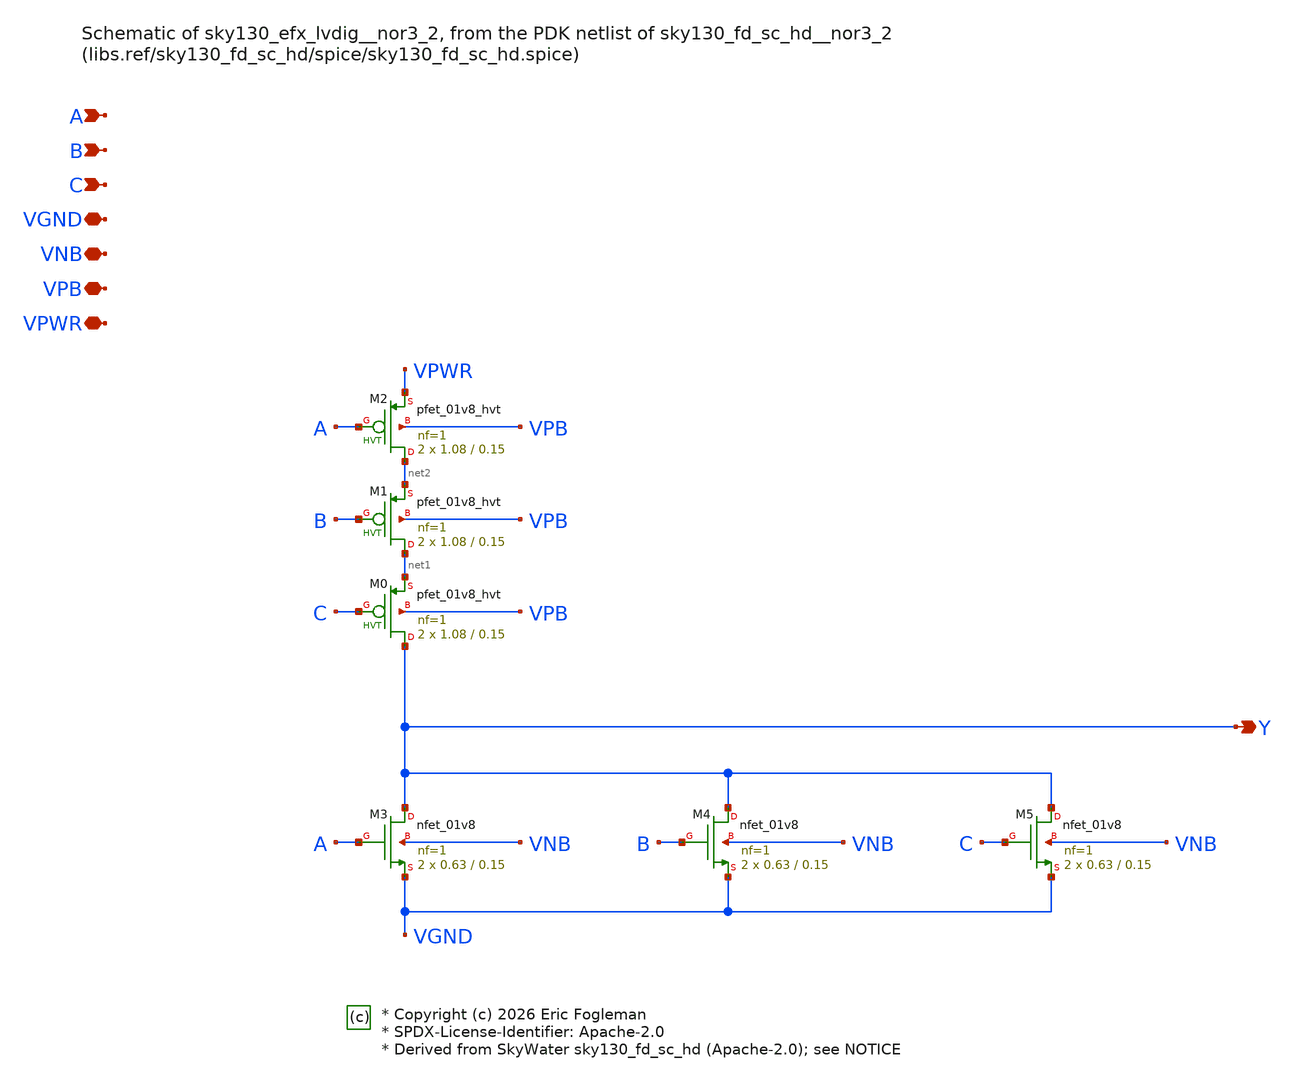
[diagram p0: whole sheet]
** sch_path: xschem/sky130_efx_lvdig__nor3_2.sch

* Copyright (c) 2026 Eric Fogleman
* SPDX-License-Identifier: Apache-2.0
* Derived from SkyWater sky130_fd_sc_hd (Apache-2.0); see NOTICE

**.subckt sky130_efx_lvdig__nor3_2 Y A B C VGND VNB VPB VPWR
*.opin Y
*.ipin A
*.ipin B
*.ipin C
*.iopin VGND
*.iopin VNB
*.iopin VPB
*.iopin VPWR
XM0 Y C net1 VPB sky130_fd_pr__pfet_01v8_hvt L=0.15 W=1.08 nf=1 ad='int((1 + 1)/2) * 1.08 / 1 * 0.29'
+ as='int((1 + 2)/2) * 1.08 / 1 * 0.29' pd='2*int((1 + 1)/2) * (1.08 / 1 + 0.29)' ps='2*int((1 + 2)/2) * (1.08 / 1 + 0.29)'
+ nrd='0.29 / 1.08 ' nrs='0.29 / 1.08 ' sa=0 sb=0 sd=0 mult=2 m=2
XM1 net1 B net2 VPB sky130_fd_pr__pfet_01v8_hvt L=0.15 W=1.08 nf=1 ad='int((1 + 1)/2) * 1.08 / 1 * 0.29'
+ as='int((1 + 2)/2) * 1.08 / 1 * 0.29' pd='2*int((1 + 1)/2) * (1.08 / 1 + 0.29)' ps='2*int((1 + 2)/2) * (1.08 / 1 + 0.29)'
+ nrd='0.29 / 1.08 ' nrs='0.29 / 1.08 ' sa=0 sb=0 sd=0 mult=2 m=2
XM2 net2 A VPWR VPB sky130_fd_pr__pfet_01v8_hvt L=0.15 W=1.08 nf=1 ad='int((1 + 1)/2) * 1.08 / 1 * 0.29'
+ as='int((1 + 2)/2) * 1.08 / 1 * 0.29' pd='2*int((1 + 1)/2) * (1.08 / 1 + 0.29)' ps='2*int((1 + 2)/2) * (1.08 / 1 + 0.29)'
+ nrd='0.29 / 1.08 ' nrs='0.29 / 1.08 ' sa=0 sb=0 sd=0 mult=2 m=2
XM3 Y A VGND VNB sky130_fd_pr__nfet_01v8 L=0.15 W=0.63 nf=1 ad='int((1 + 1)/2) * 0.63 / 1 * 0.29' as='int((1 + 2)/2) * 0.63 / 1 * 0.29'
+ pd='2*int((1 + 1)/2) * (0.63 / 1 + 0.29)' ps='2*int((1 + 2)/2) * (0.63 / 1 + 0.29)' nrd='0.29 / 0.63 '
+ nrs='0.29 / 0.63 ' sa=0 sb=0 sd=0 mult=2 m=2
XM4 Y B VGND VNB sky130_fd_pr__nfet_01v8 L=0.15 W=0.63 nf=1 ad='int((1 + 1)/2) * 0.63 / 1 * 0.29' as='int((1 + 2)/2) * 0.63 / 1 * 0.29'
+ pd='2*int((1 + 1)/2) * (0.63 / 1 + 0.29)' ps='2*int((1 + 2)/2) * (0.63 / 1 + 0.29)' nrd='0.29 / 0.63 '
+ nrs='0.29 / 0.63 ' sa=0 sb=0 sd=0 mult=2 m=2
XM5 Y C VGND VNB sky130_fd_pr__nfet_01v8 L=0.15 W=0.63 nf=1 ad='int((1 + 1)/2) * 0.63 / 1 * 0.29' as='int((1 + 2)/2) * 0.63 / 1 * 0.29'
+ pd='2*int((1 + 1)/2) * (0.63 / 1 + 0.29)' ps='2*int((1 + 2)/2) * (0.63 / 1 + 0.29)' nrd='0.29 / 0.63 '
+ nrs='0.29 / 0.63 ' sa=0 sb=0 sd=0 mult=2 m=2
**.ends
.end
